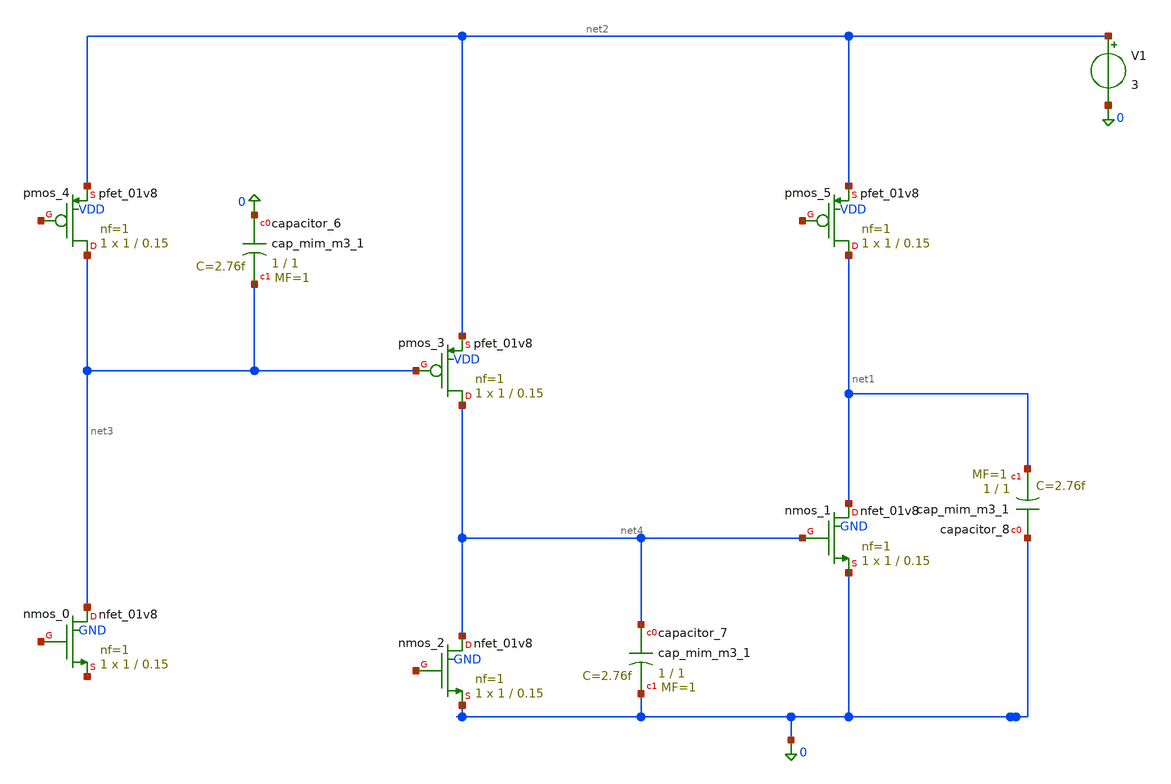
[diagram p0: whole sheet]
** sch_path: golden_netlists/10_1007_s00034-017-0630-6_05_001_crop2.sch
**.subckt 10_1007_s00034-017-0630-6_05_001_crop2
Xcapacitor_6 0 net3 sky130_fd_pr__cap_mim_m3_1 W=1 L=1 MF=1 m=1
Xcapacitor_7 net4 0 sky130_fd_pr__cap_mim_m3_1 W=1 L=1 MF=1 m=1
Xcapacitor_8 0 net1 sky130_fd_pr__cap_mim_m3_1 W=1 L=1 MF=1 m=1
Xnmos_0 net3 net5 net6 GND sky130_fd_pr__nfet_01v8 L=0.15 W=1 nf=1 ad='int((nf+1)/2) * W/nf * 0.29' as='int((nf+2)/2) * W/nf * 0.29'
+ pd='2*int((nf+1)/2) * (W/nf + 0.29)' ps='2*int((nf+2)/2) * (W/nf + 0.29)' nrd='0.29 / W' nrs='0.29 / W'
+ sa=0 sb=0 sd=0 mult=1 m=1
Xnmos_1 net1 net4 0 GND sky130_fd_pr__nfet_01v8 L=0.15 W=1 nf=1 ad='int((nf+1)/2) * W/nf * 0.29' as='int((nf+2)/2) * W/nf * 0.29'
+ pd='2*int((nf+1)/2) * (W/nf + 0.29)' ps='2*int((nf+2)/2) * (W/nf + 0.29)' nrd='0.29 / W' nrs='0.29 / W'
+ sa=0 sb=0 sd=0 mult=1 m=1
Xnmos_2 net4 net7 0 GND sky130_fd_pr__nfet_01v8 L=0.15 W=1 nf=1 ad='int((nf+1)/2) * W/nf * 0.29' as='int((nf+2)/2) * W/nf * 0.29'
+ pd='2*int((nf+1)/2) * (W/nf + 0.29)' ps='2*int((nf+2)/2) * (W/nf + 0.29)' nrd='0.29 / W' nrs='0.29 / W'
+ sa=0 sb=0 sd=0 mult=1 m=1
Xpmos_3 net4 net3 net2 VDD sky130_fd_pr__pfet_01v8 L=0.15 W=1 nf=1 ad='int((1 + 1)/2) * 1 / 1 * 0.29'
+ as='int((1 + 2)/2) * 1 / 1 * 0.29' pd='2*int((1 + 1)/2) * (1 / 1 + 0.29)' ps='2*int((1 + 2)/2) * (1 / 1 + 0.29)'
+ nrd='0.29 / 1 ' nrs='0.29 / 1 ' sa=0 sb=0 sd=0 mult=1 m=1
Xpmos_4 net3 net8 net2 VDD sky130_fd_pr__pfet_01v8 L=0.15 W=1 nf=1 ad='int((1 + 1)/2) * 1 / 1 * 0.29'
+ as='int((1 + 2)/2) * 1 / 1 * 0.29' pd='2*int((1 + 1)/2) * (1 / 1 + 0.29)' ps='2*int((1 + 2)/2) * (1 / 1 + 0.29)'
+ nrd='0.29 / 1 ' nrs='0.29 / 1 ' sa=0 sb=0 sd=0 mult=1 m=1
Xpmos_5 net1 net9 net2 VDD sky130_fd_pr__pfet_01v8 L=0.15 W=1 nf=1 ad='int((1 + 1)/2) * 1 / 1 * 0.29'
+ as='int((1 + 2)/2) * 1 / 1 * 0.29' pd='2*int((1 + 1)/2) * (1 / 1 + 0.29)' ps='2*int((1 + 2)/2) * (1 / 1 + 0.29)'
+ nrd='0.29 / 1 ' nrs='0.29 / 1 ' sa=0 sb=0 sd=0 mult=1 m=1
V1 net2 0 3
**.ends
.end
